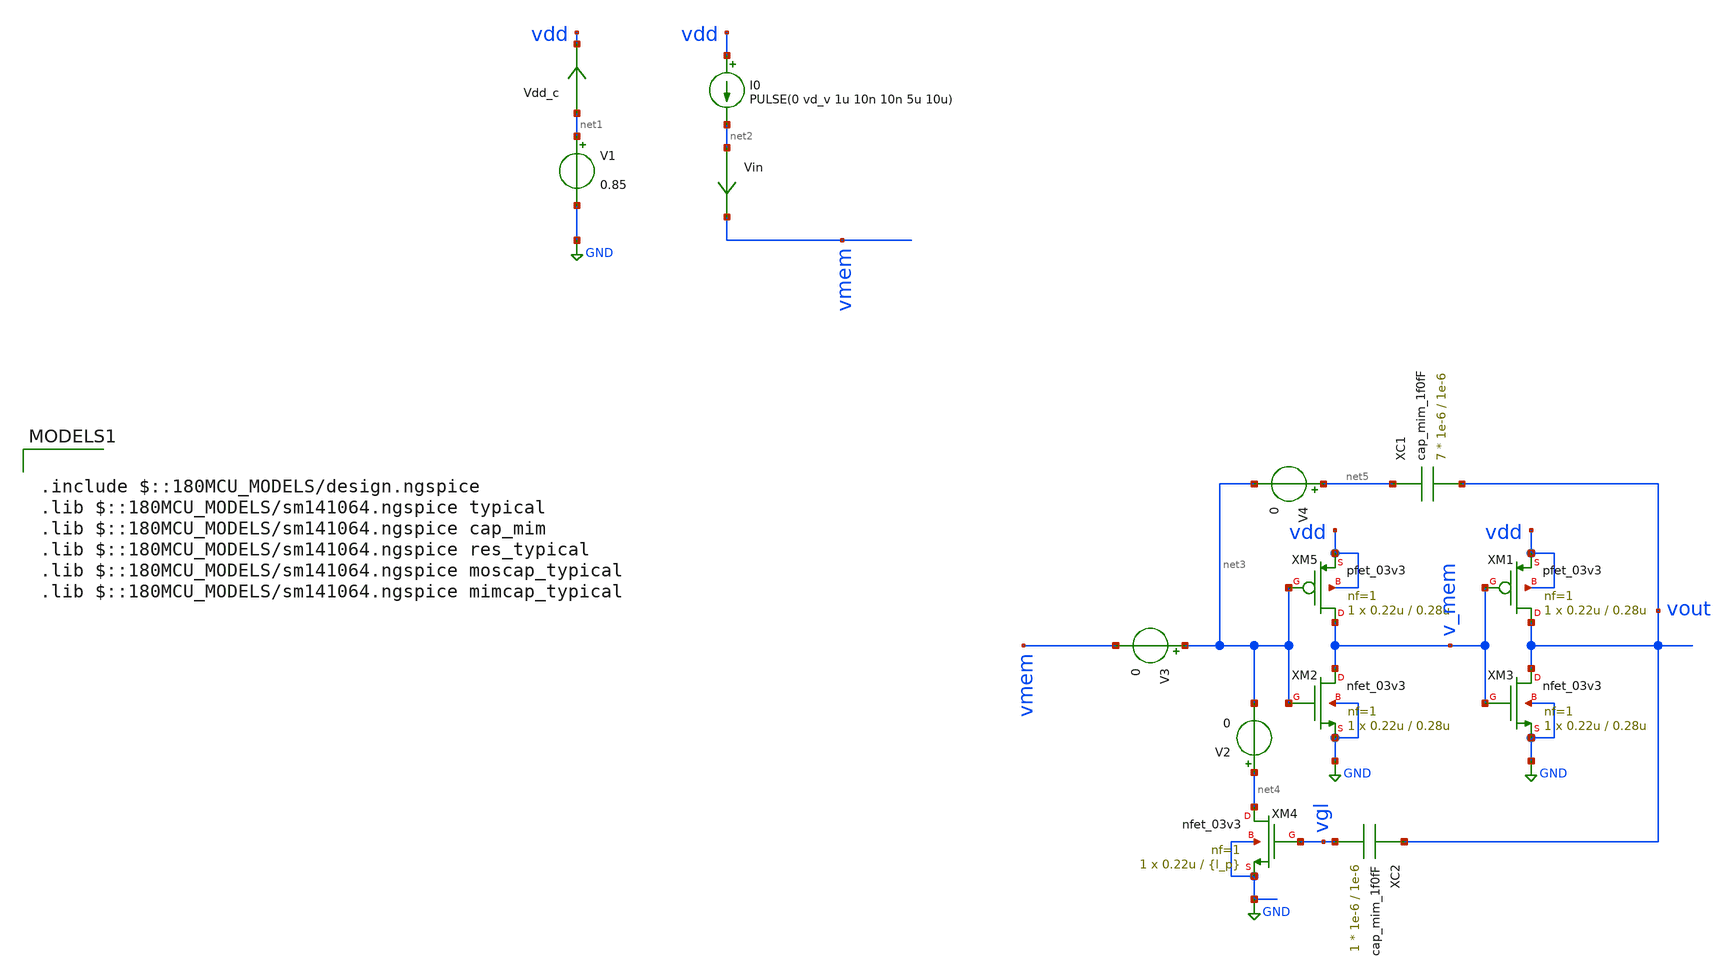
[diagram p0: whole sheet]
** sch_path: tst/AH_neuron_size.sch
**.subckt AH_neuron_size
V1 net1 GND 0.85
Vdd_c net1 vdd 0
.save i(vdd_c)
Vin net2 vmem 0
.save i(vin)
XM5 v_mem net3 vdd vdd pfet_03v3 L=0.28u W=0.22u nf=1 ad='int((nf+1)/2) * W/nf * 0.18u' as='int((nf+2)/2) * W/nf * 0.18u'
+ pd='2*int((nf+1)/2) * (W/nf + 0.18u)' ps='2*int((nf+2)/2) * (W/nf + 0.18u)' nrd='0.18u / W' nrs='0.18u / W'
+ sa=0 sb=0 sd=0 m=1
XM1 vout v_mem vdd vdd pfet_03v3 L=0.28u W=0.22u nf=1 ad='int((nf+1)/2) * W/nf * 0.18u' as='int((nf+2)/2) * W/nf * 0.18u'
+ pd='2*int((nf+1)/2) * (W/nf + 0.18u)' ps='2*int((nf+2)/2) * (W/nf + 0.18u)' nrd='0.18u / W' nrs='0.18u / W'
+ sa=0 sb=0 sd=0 m=1
XM2 v_mem net3 GND GND nfet_03v3 L=0.28u W=0.22u nf=1 ad='int((nf+1)/2) * W/nf * 0.18u' as='int((nf+2)/2) * W/nf * 0.18u'
+ pd='2*int((nf+1)/2) * (W/nf + 0.18u)' ps='2*int((nf+2)/2) * (W/nf + 0.18u)' nrd='0.18u / W' nrs='0.18u / W'
+ sa=0 sb=0 sd=0 m=1
XM3 vout v_mem GND GND nfet_03v3 L=0.28u W=0.22u nf=1 ad='int((nf+1)/2) * W/nf * 0.18u' as='int((nf+2)/2) * W/nf * 0.18u'
+ pd='2*int((nf+1)/2) * (W/nf + 0.18u)' ps='2*int((nf+2)/2) * (W/nf + 0.18u)' nrd='0.18u / W' nrs='0.18u / W'
+ sa=0 sb=0 sd=0 m=1
XC1 net5 vout cap_mim_1f0fF c_width=1e-6 c_length=1e-6 m=7
XC2 vout vgl cap_mim_1f0fF c_width=1e-6 c_length=1e-6 m=1
XM4 net4 vgl GND GND nfet_03v3 L={l_p} W=0.22u nf=1 ad='int((nf+1)/2) * W/nf * 0.18u' as='int((nf+2)/2) * W/nf * 0.18u'
+ pd='2*int((nf+1)/2) * (W/nf + 0.18u)' ps='2*int((nf+2)/2) * (W/nf + 0.18u)' nrd='0.18u / W' nrs='0.18u / W'
+ sa=0 sb=0 sd=0 m=1
V2 net4 net3 0
V3 net3 vmem 0
V4 net5 net3 0
I0 vdd net2 PULSE(0 vd_v 1u 10n 10n 5u 10u)
**** begin user architecture code


.option method=gear seed=12
.tran 100n 500m
.param vd_v=1000p
.param l_p=1u
.save allcurrents
.options save currents
.control
    let start_l=2.4u
    let stop_l=2.4u
    let delta_l=500n
    let l_act=start_l
    while l_act le stop_l
	echo Current l_p = $&l_act
	alterparam l_p = $&l_act
	reset
	save all
        run
        write sub_th_ah.raw
	let l_act=l_act+delta_l
	set appendwrite
    end
.endc



.include $::180MCU_MODELS/design.ngspice
.lib $::180MCU_MODELS/sm141064.ngspice typical
.lib $::180MCU_MODELS/sm141064.ngspice cap_mim
.lib $::180MCU_MODELS/sm141064.ngspice res_typical
.lib $::180MCU_MODELS/sm141064.ngspice moscap_typical
.lib $::180MCU_MODELS/sm141064.ngspice mimcap_typical

**** end user architecture code
**.ends
.GLOBAL GND
.end
